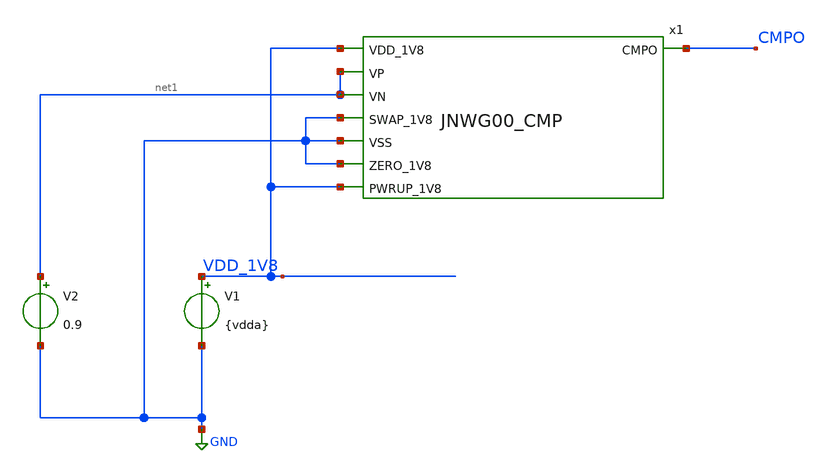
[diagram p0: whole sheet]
** sch_path: design/JNW_GR00_SKY130NM/TB_CMP.sch
**.subckt TB_CMP
V1 VDD_1V8 GND {vdda}
V2 net1 GND 0.9
x1 VDD_1V8 net1 CMPO net1 GND GND GND VDD_1V8 JNWG00_CMP
**** begin user architecture code



* ngspice commands
.include corner.spi



**** end user architecture code
**.ends
.GLOBAL GND
.end
